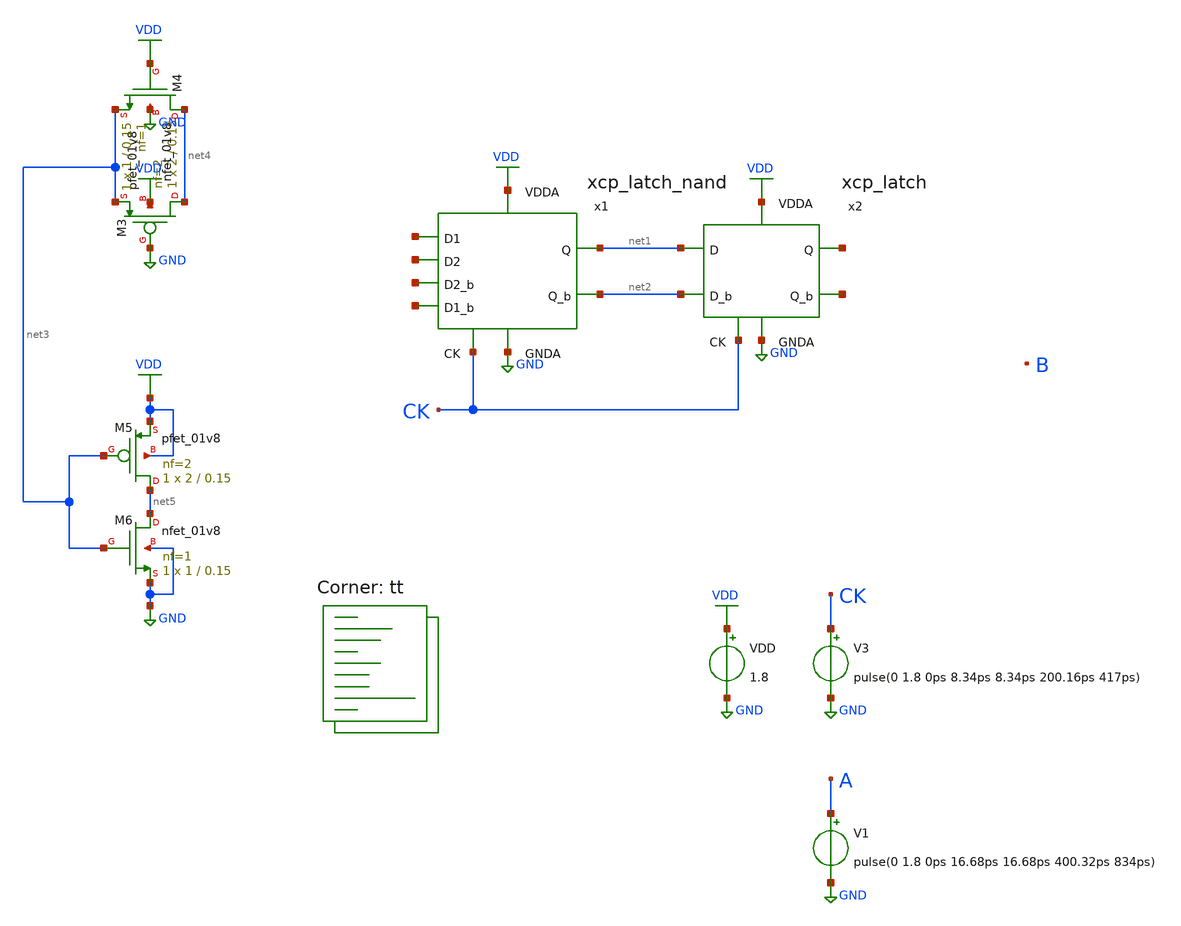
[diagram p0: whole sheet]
** sch_path: projects/pll/divider/xschem_ngspice/tb_xcp_latch_divide3.sch
**.subckt tb_xcp_latch_divide3
VDD VDD GND 1.8
V3 CK GND pulse(0 1.8 0ps 8.34ps 8.34ps 200.16ps 417ps)
V1 A GND pulse(0 1.8 0ps 16.68ps 16.68ps 400.32ps 834ps)
x1 VDD net2 net1 net6 net7 net8 net9 CK GND xcp_latch_nand
x2 VDD net10 net11 net2 net1 CK GND xcp_latch
XM3 net4 GND net3 VDD sky130_fd_pr__pfet_01v8 L=0.15 W=2 nf=2 ad='int((nf+1)/2) * W/nf * 0.29' as='int((nf+2)/2) * W/nf * 0.29'
+ pd='2*int((nf+1)/2) * (W/nf + 0.29)' ps='2*int((nf+2)/2) * (W/nf + 0.29)' nrd='0.29 / W' nrs='0.29 / W'
+ sa=0 sb=0 sd=0 mult=1 m=1
XM4 net4 VDD net3 GND sky130_fd_pr__nfet_01v8 L=0.15 W=1 nf=1 ad='int((nf+1)/2) * W/nf * 0.29' as='int((nf+2)/2) * W/nf * 0.29'
+ pd='2*int((nf+1)/2) * (W/nf + 0.29)' ps='2*int((nf+2)/2) * (W/nf + 0.29)' nrd='0.29 / W' nrs='0.29 / W'
+ sa=0 sb=0 sd=0 mult=1 m=1
XM5 net5 net3 VDD VDD sky130_fd_pr__pfet_01v8 L=0.15 W=2 nf=2 ad='int((nf+1)/2) * W/nf * 0.29' as='int((nf+2)/2) * W/nf * 0.29'
+ pd='2*int((nf+1)/2) * (W/nf + 0.29)' ps='2*int((nf+2)/2) * (W/nf + 0.29)' nrd='0.29 / W' nrs='0.29 / W'
+ sa=0 sb=0 sd=0 mult=1 m=1
XM6 net5 net3 GND GND sky130_fd_pr__nfet_01v8 L=0.15 W=1 nf=1 ad='int((nf+1)/2) * W/nf * 0.29' as='int((nf+2)/2) * W/nf * 0.29'
+ pd='2*int((nf+1)/2) * (W/nf + 0.29)' ps='2*int((nf+2)/2) * (W/nf + 0.29)' nrd='0.29 / W' nrs='0.29 / W'
+ sa=0 sb=0 sd=0 mult=1 m=1
**** begin user architecture code



.include /foss/pdks/sky130A/libs.ref/sky130_fd_sc_hd/spice/sky130_fd_sc_hd.spice

.option method=gear
.option wnflag=1
* .option savecurrents

.save @m.x1.xm1.msky130_fd_pr__nfet_01v8[gm] @m.x1.xm2.msky130_fd_pr__nfet_01v8[gm] @m.x1.xm3.msky130_fd_pr__pfet_01v8[gm] @m.x1.xm4.msky130_fd_pr__pfet_01v8[gm] @m.x1.xm5.msky130_fd_pr__nfet_01v8[gm] @m.x2.xm1.msky130_fd_pr__nfet_01v8[gm] @m.x2.xm2.msky130_fd_pr__nfet_01v8[gm] @m.x2.xm3.msky130_fd_pr__pfet_01v8[gm] @m.x2.xm4.msky130_fd_pr__pfet_01v8[gm] @m.x2.xm5.msky130_fd_pr__nfet_01v8[gm] @v.x1.vmeas @v.x1.vmeas1 @v.x1.vmeas2 @v.x5.vmeas @v.x5.vmeas1 @v.x5.vmeas2


*.ic v(b)=0

.control

  save v(a) v(a_b) v(b) v(b_b) v(c) v(ck)
  * save all
  *tran 0.1n 1u
  tran 0.2p 10n
  *ac dec 20 1 1T
  remzerovec
  write tb_xcp_latch_divide3.raw
  set appendwrite

.endc



.lib $::SKYWATER_MODELS/sky130.lib.spice tt
**** end user architecture code
**.ends

* expanding   symbol:
*+  /foss/designs/my_design/projects/pll/divider/xschem_ngspice/xcp_latch_nand.sym # of pins=9
** sym_path: projects/pll/divider/xschem_ngspice/xcp_latch_nand.sym
** sch_path: projects/pll/divider/xschem_ngspice/xcp_latch_nand.sch
.subckt xcp_latch_nand VDDA Q_b Q D1 D1_b D2_b D2 CK GNDA
*.ipin D2
*.opin Q
*.ipin D1_b
*.ipin CK
*.opin Q_b
*.ipin VDDA
*.ipin GNDA
*.ipin D1
*.ipin D2_b
XM5 net1 CK GNDA GNDA sky130_fd_pr__nfet_01v8 L=0.15 W=2 nf=2 ad='int((nf+1)/2) * W/nf * 0.29' as='int((nf+2)/2) * W/nf * 0.29'
+ pd='2*int((nf+1)/2) * (W/nf + 0.29)' ps='2*int((nf+2)/2) * (W/nf + 0.29)' nrd='0.29 / W' nrs='0.29 / W'
+ sa=0 sb=0 sd=0 mult=1 m=1
XM1 net4 D2 V_common GNDA sky130_fd_pr__nfet_01v8 L=0.15 W=1 nf=1 ad='int((nf+1)/2) * W/nf * 0.29' as='int((nf+2)/2) * W/nf * 0.29'
+ pd='2*int((nf+1)/2) * (W/nf + 0.29)' ps='2*int((nf+2)/2) * (W/nf + 0.29)' nrd='0.29 / W' nrs='0.29 / W'
+ sa=0 sb=0 sd=0 mult=1 m=1
XM2 net2 D1_b V_common GNDA sky130_fd_pr__nfet_01v8 L=0.15 W=1 nf=1 ad='int((nf+1)/2) * W/nf * 0.29'
+ as='int((nf+2)/2) * W/nf * 0.29' pd='2*int((nf+1)/2) * (W/nf + 0.29)' ps='2*int((nf+2)/2) * (W/nf + 0.29)'
+ nrd='0.29 / W' nrs='0.29 / W' sa=0 sb=0 sd=0 mult=1 m=1
Vmeas V_common net1 0
.save i(vmeas)
Vmeas1 Q_b net3 0
.save i(vmeas1)
Vmeas2 Q net2 0
.save i(vmeas2)
XM3 Q_b Q VDDA VDDA sky130_fd_pr__pfet_01v8 L=0.15 W=1 nf=1 ad='int((nf+1)/2) * W/nf * 0.29' as='int((nf+2)/2) * W/nf * 0.29'
+ pd='2*int((nf+1)/2) * (W/nf + 0.29)' ps='2*int((nf+2)/2) * (W/nf + 0.29)' nrd='0.29 / W' nrs='0.29 / W'
+ sa=0 sb=0 sd=0 mult=1 m=1
XM4 Q Q_b VDDA VDDA sky130_fd_pr__pfet_01v8 L=0.15 W=1 nf=1 ad='int((nf+1)/2) * W/nf * 0.29' as='int((nf+2)/2) * W/nf * 0.29'
+ pd='2*int((nf+1)/2) * (W/nf + 0.29)' ps='2*int((nf+2)/2) * (W/nf + 0.29)' nrd='0.29 / W' nrs='0.29 / W'
+ sa=0 sb=0 sd=0 mult=1 m=1
XM6 net3 D1 net4 GNDA sky130_fd_pr__nfet_01v8 L=0.15 W=1 nf=1 ad='int((nf+1)/2) * W/nf * 0.29' as='int((nf+2)/2) * W/nf * 0.29'
+ pd='2*int((nf+1)/2) * (W/nf + 0.29)' ps='2*int((nf+2)/2) * (W/nf + 0.29)' nrd='0.29 / W' nrs='0.29 / W'
+ sa=0 sb=0 sd=0 mult=1 m=1
XM7 net2 D2_b V_common GNDA sky130_fd_pr__nfet_01v8 L=0.15 W=1 nf=1 ad='int((nf+1)/2) * W/nf * 0.29'
+ as='int((nf+2)/2) * W/nf * 0.29' pd='2*int((nf+1)/2) * (W/nf + 0.29)' ps='2*int((nf+2)/2) * (W/nf + 0.29)'
+ nrd='0.29 / W' nrs='0.29 / W' sa=0 sb=0 sd=0 mult=1 m=1
.ends


* expanding   symbol:  /foss/designs/my_design/projects/pll/divider/xschem_ngspice/xcp_latch.sym #
*+ of pins=7
** sym_path: projects/pll/divider/xschem_ngspice/xcp_latch.sym
** sch_path: projects/pll/divider/xschem_ngspice/xcp_latch.sch
.subckt xcp_latch VDDA Q_b Q D_b D CK GNDA
*.ipin D
*.opin Q
*.ipin D_b
*.ipin CK
*.opin Q_b
*.ipin VDDA
*.ipin GNDA
XM5 net1 CK GNDA GNDA sky130_fd_pr__nfet_01v8 L=0.15 W=2 nf=2 ad='int((nf+1)/2) * W/nf * 0.29' as='int((nf+2)/2) * W/nf * 0.29'
+ pd='2*int((nf+1)/2) * (W/nf + 0.29)' ps='2*int((nf+2)/2) * (W/nf + 0.29)' nrd='0.29 / W' nrs='0.29 / W'
+ sa=0 sb=0 sd=0 mult=1 m=1
XM1 net3 D V_common GNDA sky130_fd_pr__nfet_01v8 L=0.15 W=1 nf=1 ad='int((nf+1)/2) * W/nf * 0.29' as='int((nf+2)/2) * W/nf * 0.29'
+ pd='2*int((nf+1)/2) * (W/nf + 0.29)' ps='2*int((nf+2)/2) * (W/nf + 0.29)' nrd='0.29 / W' nrs='0.29 / W'
+ sa=0 sb=0 sd=0 mult=1 m=1
XM2 net2 D_b V_common GNDA sky130_fd_pr__nfet_01v8 L=0.15 W=1 nf=1 ad='int((nf+1)/2) * W/nf * 0.29' as='int((nf+2)/2) * W/nf * 0.29'
+ pd='2*int((nf+1)/2) * (W/nf + 0.29)' ps='2*int((nf+2)/2) * (W/nf + 0.29)' nrd='0.29 / W' nrs='0.29 / W'
+ sa=0 sb=0 sd=0 mult=1 m=1
Vmeas V_common net1 0
.save i(vmeas)
Vmeas1 Q_b net3 0
.save i(vmeas1)
Vmeas2 Q net2 0
.save i(vmeas2)
XM3 Q_b Q VDDA VDDA sky130_fd_pr__pfet_01v8 L=0.15 W=1 nf=1 ad='int((nf+1)/2) * W/nf * 0.29' as='int((nf+2)/2) * W/nf * 0.29'
+ pd='2*int((nf+1)/2) * (W/nf + 0.29)' ps='2*int((nf+2)/2) * (W/nf + 0.29)' nrd='0.29 / W' nrs='0.29 / W'
+ sa=0 sb=0 sd=0 mult=1 m=1
XM4 Q Q_b VDDA VDDA sky130_fd_pr__pfet_01v8 L=0.15 W=1 nf=1 ad='int((nf+1)/2) * W/nf * 0.29' as='int((nf+2)/2) * W/nf * 0.29'
+ pd='2*int((nf+1)/2) * (W/nf + 0.29)' ps='2*int((nf+2)/2) * (W/nf + 0.29)' nrd='0.29 / W' nrs='0.29 / W'
+ sa=0 sb=0 sd=0 mult=1 m=1
.ends

.GLOBAL GND
.GLOBAL VDD
.end
